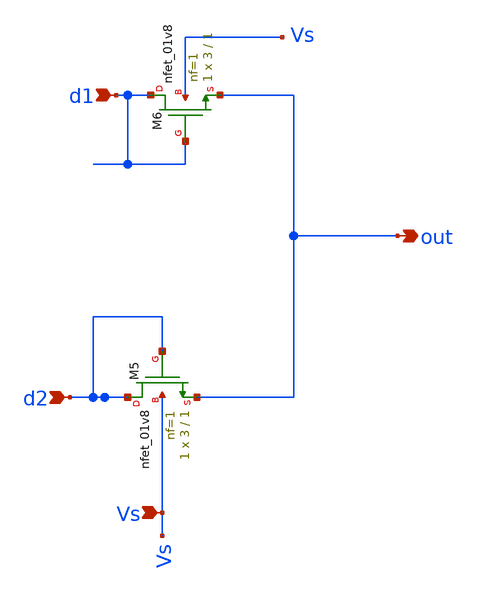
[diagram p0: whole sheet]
** sch_path: xschem/nmos_diode_connected.sch
**.subckt nmos_diode_connected out Vs d2 d1
*.opin out
*.ipin Vs
*.ipin d2
*.ipin d1
XM5 d2 d2 out Vs sky130_fd_pr__nfet_01v8 L=1 W=3 nf=1 ad='int((nf+1)/2) * W/nf * 0.29' as='int((nf+2)/2) * W/nf * 0.29'
+ pd='2*int((nf+1)/2) * (W/nf + 0.29)' ps='2*int((nf+2)/2) * (W/nf + 0.29)' nrd='0.29 / W' nrs='0.29 / W'
+ sa=0 sb=0 sd=0 mult=1 m=1
XM6 d1 d1 out Vs sky130_fd_pr__nfet_01v8 L=1 W=3 nf=1 ad='int((nf+1)/2) * W/nf * 0.29' as='int((nf+2)/2) * W/nf * 0.29'
+ pd='2*int((nf+1)/2) * (W/nf + 0.29)' ps='2*int((nf+2)/2) * (W/nf + 0.29)' nrd='0.29 / W' nrs='0.29 / W'
+ sa=0 sb=0 sd=0 mult=1 m=1
**.ends
.end
